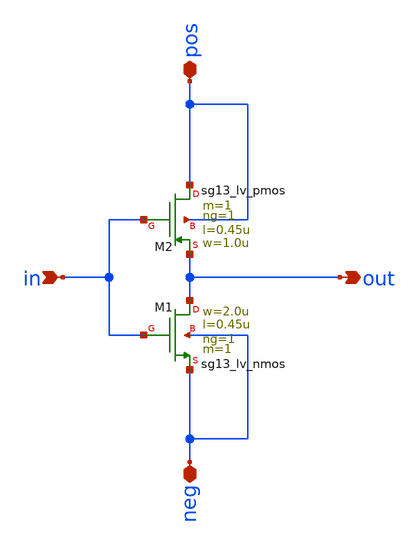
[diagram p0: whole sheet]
** sch_path: analog/inverter/inverter.sch
**.subckt inverter in pos neg out
*.ipin in
*.iopin pos
*.iopin neg
*.opin out
XM1 out in neg neg sg13_lv_nmos w=2.0u l=0.45u ng=1 m=1 mm_ok=1
XM2 pos in out pos sg13_lv_pmos w=1.0u l=0.45u ng=1 m=1 mm_ok=1
**.ends
.end
